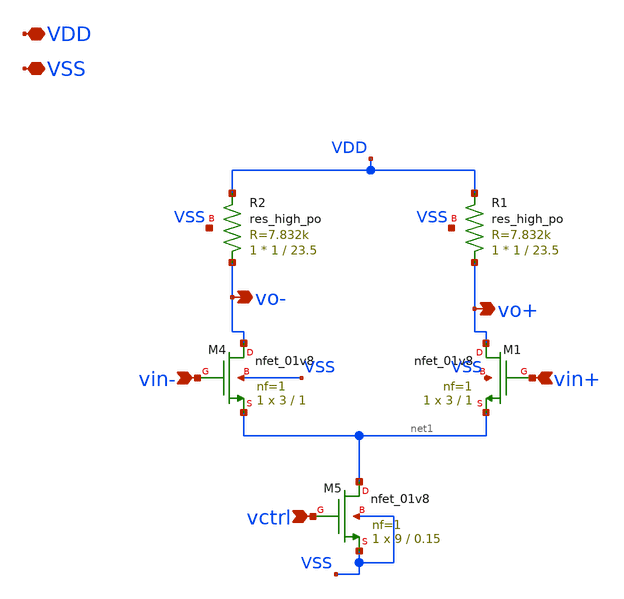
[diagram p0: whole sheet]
** sch_path: xschem/tuning/ring_inverter_tune.sch
**.subckt ring_inverter_tune VDD VSS vo+ vin- vctrl vo- vin+
*.iopin VDD
*.iopin VSS
*.opin vo+
*.ipin vin-
*.ipin vctrl
*.opin vo-
*.ipin vin+
XM4 vo- vin- net1 VSS sky130_fd_pr__nfet_01v8 L=1 W=3 nf=1 ad='int((nf+1)/2) * W/nf * 0.29' as='int((nf+2)/2) * W/nf * 0.29'
+ pd='2*int((nf+1)/2) * (W/nf + 0.29)' ps='2*int((nf+2)/2) * (W/nf + 0.29)' nrd='0.29 / W' nrs='0.29 / W'
+ sa=0 sb=0 sd=0 mult=1 m=1
XM5 net1 vctrl VSS VSS sky130_fd_pr__nfet_01v8 L=0.15 W=9 nf=1 ad='int((nf+1)/2) * W/nf * 0.29' as='int((nf+2)/2) * W/nf * 0.29'
+ pd='2*int((nf+1)/2) * (W/nf + 0.29)' ps='2*int((nf+2)/2) * (W/nf + 0.29)' nrd='0.29 / W' nrs='0.29 / W'
+ sa=0 sb=0 sd=0 mult=1 m=1
XM1 vo+ vin+ net1 VSS sky130_fd_pr__nfet_01v8 L=1 W=3 nf=1 ad='int((nf+1)/2) * W/nf * 0.29' as='int((nf+2)/2) * W/nf * 0.29'
+ pd='2*int((nf+1)/2) * (W/nf + 0.29)' ps='2*int((nf+2)/2) * (W/nf + 0.29)' nrd='0.29 / W' nrs='0.29 / W'
+ sa=0 sb=0 sd=0 mult=1 m=1
XR1 vo+ VDD VSS sky130_fd_pr__res_high_po W=1 L=23.5 mult=1 m=1
XR2 vo- VDD VSS sky130_fd_pr__res_high_po W=1 L=23.5 mult=1 m=1
**.ends
.end
